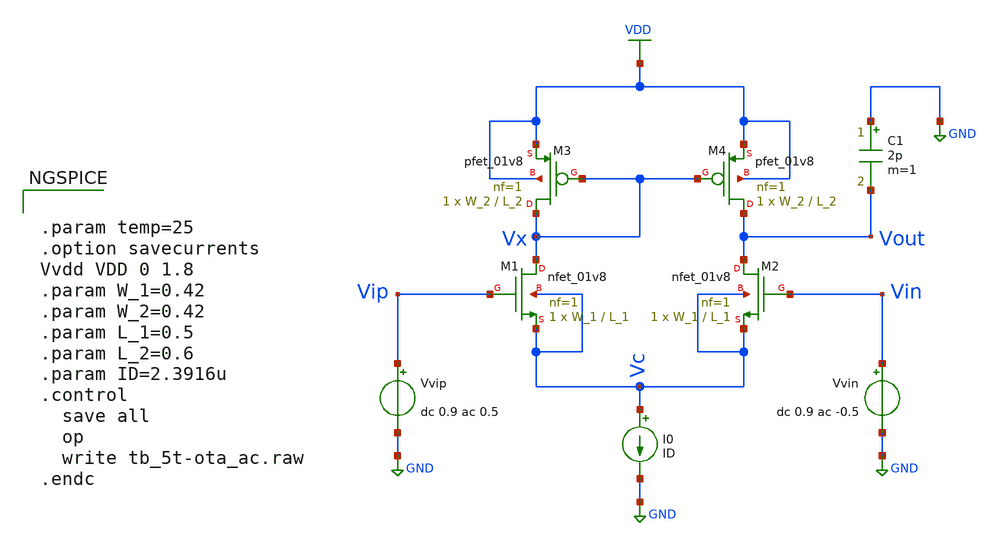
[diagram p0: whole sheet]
** sch_path: Xschem Simulations/5T-OTA/tb_5t-ota_ac.sch
**.subckt tb_5t-ota_ac
XM1 Vx Vip Vc Vc sky130_fd_pr__nfet_01v8 L=L_1 W=W_1 nf=1 ad='int((1 + 1)/2) * W_1 / 1 * 0.29' as='int((1 + 2)/2) * W_1 / 1 * 0.29'
+ pd='2*int((1 + 1)/2) * (W_1 / 1 + 0.29)' ps='2*int((1 + 2)/2) * (W_1 / 1 + 0.29)' nrd='0.29 / W_1 ' nrs='0.29 / W_1 '
+ sa=0 sb=0 sd=0 mult=1 m=1
XM2 Vout Vin Vc Vc sky130_fd_pr__nfet_01v8 L=L_1 W=W_1 nf=1 ad='int((1 + 1)/2) * W_1 / 1 * 0.29' as='int((1 + 2)/2) * W_1 / 1 * 0.29'
+ pd='2*int((1 + 1)/2) * (W_1 / 1 + 0.29)' ps='2*int((1 + 2)/2) * (W_1 / 1 + 0.29)' nrd='0.29 / W_1 ' nrs='0.29 / W_1 '
+ sa=0 sb=0 sd=0 mult=1 m=1
I0 Vc GND ID
Vvip Vip GND dc 0.9 ac 0.5
Vvin Vin GND dc 0.9 ac -0.5
C1 GND Vout 2p m=1
XM3 Vx Vx VDD VDD sky130_fd_pr__pfet_01v8 L=L_2 W=W_2 nf=1 ad='int((1 + 1)/2) * W_2 / 1 * 0.29' as='int((1 + 2)/2) * W_2 / 1 * 0.29'
+ pd='2*int((1 + 1)/2) * (W_2 / 1 + 0.29)' ps='2*int((1 + 2)/2) * (W_2 / 1 + 0.29)' nrd='0.29 / W_2 ' nrs='0.29 / W_2 '
+ sa=0 sb=0 sd=0 mult=1 m=1
XM4 Vout Vx VDD VDD sky130_fd_pr__pfet_01v8 L=L_2 W=W_2 nf=1 ad='int((1 + 1)/2) * W_2 / 1 * 0.29' as='int((1 + 2)/2) * W_2 / 1 * 0.29'
+ pd='2*int((1 + 1)/2) * (W_2 / 1 + 0.29)' ps='2*int((1 + 2)/2) * (W_2 / 1 + 0.29)' nrd='0.29 / W_2 ' nrs='0.29 / W_2 '
+ sa=0 sb=0 sd=0 mult=1 m=1
**** begin user architecture code

** opencircuitdesign pdks install
.lib $::SKYWATER_MODELS/sky130.lib.spice tt



.param temp=25
.option savecurrents
Vvdd VDD 0 1.8
.param W_1=0.42
.param W_2=0.42
.param L_1=0.5
.param L_2=0.6
.param ID=2.3916u
.control
  save all
  op
  write tb_5t-ota_ac.raw
.endc




.control
  ac dec 20 0.1 1G
  save all

  let gain = v(vout) / (v(vip) - v(vin))
  let db_gain = db(gain)
  let deg_phase = 180*cph(v(vout))/pi

  meas ac gain_DC FIND db_gain AT=1

  meas ac gbw_freq WHEN db_gain=0 FALL=1
  let gbw_Mfreq = gbw_freq * 1e-6

  meas ac pm_deg FIND deg_phase AT=gbw_freq
  let pm = 180 + pm_deg

  plot db_gain deg_phase
  print gain_DC
  print gbw_Mfreq
  print pm
.endc


**** end user architecture code
**.ends
.GLOBAL GND
.GLOBAL VDD
.end
